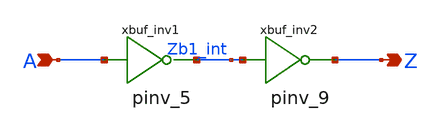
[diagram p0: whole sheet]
** sch_path: sram_4_16_scn4m/pdriver_3.sch
**.subckt pdriver_3 A Z
*.ipin A
*.opin Z
xbuf_inv1 A Zb1_int vdd gnd pinv_5
xbuf_inv2 Zb1_int Z vdd gnd pinv_9
**.ends

* expanding   symbol:  pinv_5.sym # of pins=2
** sym_path: sram_2_16_scn4m/pinv_5.sym
** sch_path: sram_2_16_scn4m/pinv_5.sch
.subckt pinv_5 A Z vdd gnd
*.ipin A
*.opin Z
Mpinv_nmos Z A gnd gnd n w=0.8u l=0.4u m=1
Mp_inv_pmos Z A vdd vdd p w=1.6u l=0.4u m=1
.ends


* expanding   symbol:  pinv_9.sym # of pins=2
** sym_path: sram_2_16_scn4m/pinv_9.sym
** sch_path: sram_2_16_scn4m/pinv_9.sch
.subckt pinv_9 A Z vdd gnd
*.ipin A
*.opin Z
Mpinv_nmos Z A gnd gnd n w=4.0u l=0.4u m=2
Mp_inv_pmos Z A vdd vdd p w=8.0u l=0.4u m=2
.ends

.end
